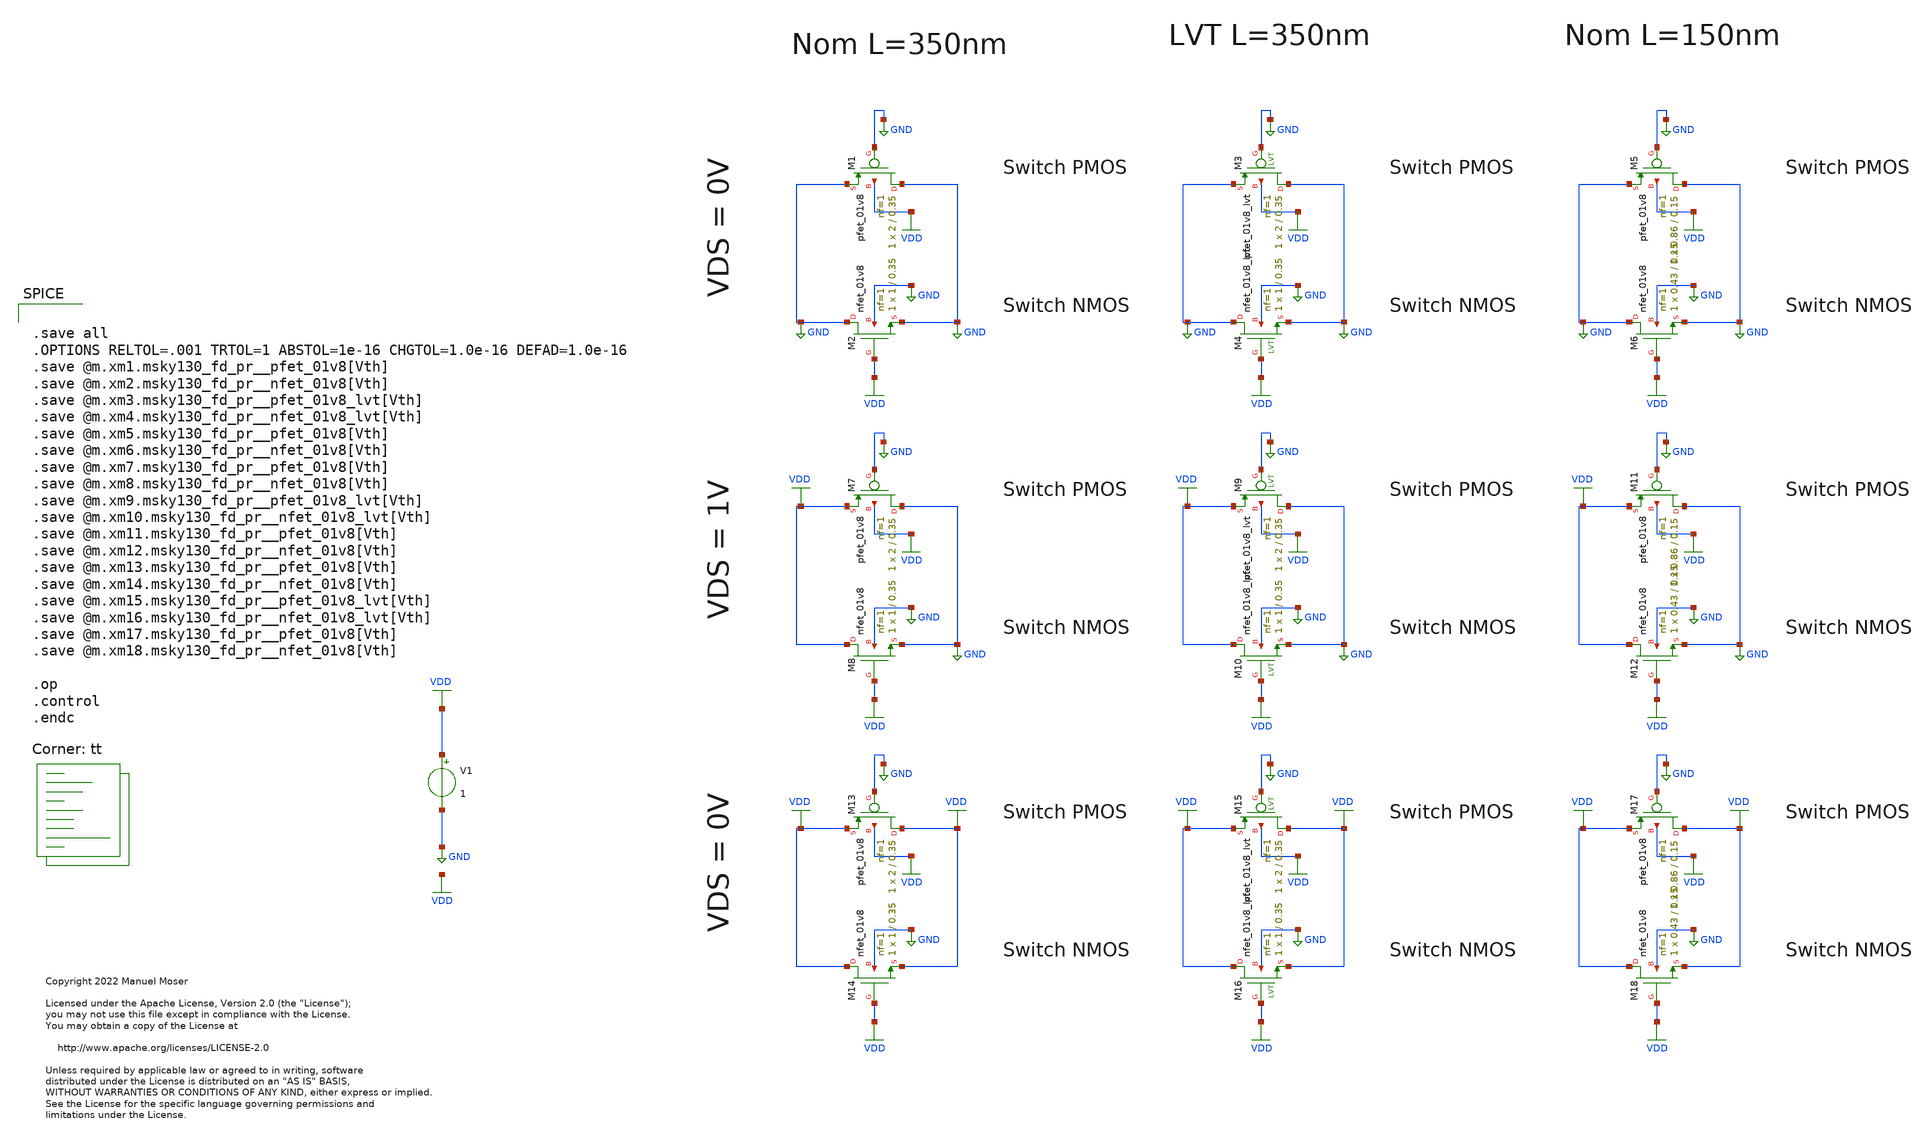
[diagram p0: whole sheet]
** sch_path: xschem/switch/switch_vth_tb.sch
* Copyright 2022 Manuel Moser
* Licensed under the Apache License, Version 2.0 (the "License");
**.subckt switch_vth_tb
V1 VDD GND 1
XM2 GND VDD GND GND sky130_fd_pr__nfet_01v8 L=0.35 W=1 nf=1 ad='int((nf+1)/2) * W/nf * 0.29' as='int((nf+2)/2) * W/nf * 0.29'
+ pd='2*int((nf+1)/2) * (W/nf + 0.29)' ps='2*int((nf+2)/2) * (W/nf + 0.29)' nrd='0.29 / W' nrs='0.29 / W'
+ sa=0 sb=0 sd=0 mult=1 m=1
XM1 GND GND GND VDD sky130_fd_pr__pfet_01v8 L=0.35 W=2 nf=1 ad='int((nf+1)/2) * W/nf * 0.29' as='int((nf+2)/2) * W/nf * 0.29'
+ pd='2*int((nf+1)/2) * (W/nf + 0.29)' ps='2*int((nf+2)/2) * (W/nf + 0.29)' nrd='0.29 / W' nrs='0.29 / W'
+ sa=0 sb=0 sd=0 mult=1 m=1
XM3 GND GND GND VDD sky130_fd_pr__pfet_01v8_lvt L=0.35 W=2 nf=1 ad='int((nf+1)/2) * W/nf * 0.29' as='int((nf+2)/2) * W/nf * 0.29'
+ pd='2*int((nf+1)/2) * (W/nf + 0.29)' ps='2*int((nf+2)/2) * (W/nf + 0.29)' nrd='0.29 / W' nrs='0.29 / W'
+ sa=0 sb=0 sd=0 mult=1 m=1
XM4 GND VDD GND GND sky130_fd_pr__nfet_01v8_lvt L=0.35 W=1 nf=1 ad='int((nf+1)/2) * W/nf * 0.29' as='int((nf+2)/2) * W/nf * 0.29'
+ pd='2*int((nf+1)/2) * (W/nf + 0.29)' ps='2*int((nf+2)/2) * (W/nf + 0.29)' nrd='0.29 / W' nrs='0.29 / W'
+ sa=0 sb=0 sd=0 mult=1 m=1
XM6 GND VDD GND GND sky130_fd_pr__nfet_01v8 L=0.15 W=0.43 nf=1 ad='int((nf+1)/2) * W/nf * 0.29' as='int((nf+2)/2) * W/nf * 0.29'
+ pd='2*int((nf+1)/2) * (W/nf + 0.29)' ps='2*int((nf+2)/2) * (W/nf + 0.29)' nrd='0.29 / W' nrs='0.29 / W'
+ sa=0 sb=0 sd=0 mult=1 m=1
XM5 GND GND GND VDD sky130_fd_pr__pfet_01v8 L=0.15 W=0.86 nf=1 ad='int((nf+1)/2) * W/nf * 0.29' as='int((nf+2)/2) * W/nf * 0.29'
+ pd='2*int((nf+1)/2) * (W/nf + 0.29)' ps='2*int((nf+2)/2) * (W/nf + 0.29)' nrd='0.29 / W' nrs='0.29 / W'
+ sa=0 sb=0 sd=0 mult=1 m=1
XM8 VDD VDD GND GND sky130_fd_pr__nfet_01v8 L=0.35 W=1 nf=1 ad='int((nf+1)/2) * W/nf * 0.29' as='int((nf+2)/2) * W/nf * 0.29'
+ pd='2*int((nf+1)/2) * (W/nf + 0.29)' ps='2*int((nf+2)/2) * (W/nf + 0.29)' nrd='0.29 / W' nrs='0.29 / W'
+ sa=0 sb=0 sd=0 mult=1 m=1
XM7 GND GND VDD VDD sky130_fd_pr__pfet_01v8 L=0.35 W=2 nf=1 ad='int((nf+1)/2) * W/nf * 0.29' as='int((nf+2)/2) * W/nf * 0.29'
+ pd='2*int((nf+1)/2) * (W/nf + 0.29)' ps='2*int((nf+2)/2) * (W/nf + 0.29)' nrd='0.29 / W' nrs='0.29 / W'
+ sa=0 sb=0 sd=0 mult=1 m=1
XM9 GND GND VDD VDD sky130_fd_pr__pfet_01v8_lvt L=0.35 W=2 nf=1 ad='int((nf+1)/2) * W/nf * 0.29' as='int((nf+2)/2) * W/nf * 0.29'
+ pd='2*int((nf+1)/2) * (W/nf + 0.29)' ps='2*int((nf+2)/2) * (W/nf + 0.29)' nrd='0.29 / W' nrs='0.29 / W'
+ sa=0 sb=0 sd=0 mult=1 m=1
XM10 VDD VDD GND GND sky130_fd_pr__nfet_01v8_lvt L=0.35 W=1 nf=1 ad='int((nf+1)/2) * W/nf * 0.29' as='int((nf+2)/2) * W/nf * 0.29'
+ pd='2*int((nf+1)/2) * (W/nf + 0.29)' ps='2*int((nf+2)/2) * (W/nf + 0.29)' nrd='0.29 / W' nrs='0.29 / W'
+ sa=0 sb=0 sd=0 mult=1 m=1
XM12 VDD VDD GND GND sky130_fd_pr__nfet_01v8 L=0.15 W=0.43 nf=1 ad='int((nf+1)/2) * W/nf * 0.29' as='int((nf+2)/2) * W/nf * 0.29'
+ pd='2*int((nf+1)/2) * (W/nf + 0.29)' ps='2*int((nf+2)/2) * (W/nf + 0.29)' nrd='0.29 / W' nrs='0.29 / W'
+ sa=0 sb=0 sd=0 mult=1 m=1
XM11 GND GND VDD VDD sky130_fd_pr__pfet_01v8 L=0.15 W=0.86 nf=1 ad='int((nf+1)/2) * W/nf * 0.29' as='int((nf+2)/2) * W/nf * 0.29'
+ pd='2*int((nf+1)/2) * (W/nf + 0.29)' ps='2*int((nf+2)/2) * (W/nf + 0.29)' nrd='0.29 / W' nrs='0.29 / W'
+ sa=0 sb=0 sd=0 mult=1 m=1
XM14 VDD VDD VDD GND sky130_fd_pr__nfet_01v8 L=0.35 W=1 nf=1 ad='int((nf+1)/2) * W/nf * 0.29' as='int((nf+2)/2) * W/nf * 0.29'
+ pd='2*int((nf+1)/2) * (W/nf + 0.29)' ps='2*int((nf+2)/2) * (W/nf + 0.29)' nrd='0.29 / W' nrs='0.29 / W'
+ sa=0 sb=0 sd=0 mult=1 m=1
XM13 VDD GND VDD VDD sky130_fd_pr__pfet_01v8 L=0.35 W=2 nf=1 ad='int((nf+1)/2) * W/nf * 0.29' as='int((nf+2)/2) * W/nf * 0.29'
+ pd='2*int((nf+1)/2) * (W/nf + 0.29)' ps='2*int((nf+2)/2) * (W/nf + 0.29)' nrd='0.29 / W' nrs='0.29 / W'
+ sa=0 sb=0 sd=0 mult=1 m=1
XM15 VDD GND VDD VDD sky130_fd_pr__pfet_01v8_lvt L=0.35 W=2 nf=1 ad='int((nf+1)/2) * W/nf * 0.29' as='int((nf+2)/2) * W/nf * 0.29'
+ pd='2*int((nf+1)/2) * (W/nf + 0.29)' ps='2*int((nf+2)/2) * (W/nf + 0.29)' nrd='0.29 / W' nrs='0.29 / W'
+ sa=0 sb=0 sd=0 mult=1 m=1
XM16 VDD VDD VDD GND sky130_fd_pr__nfet_01v8_lvt L=0.35 W=1 nf=1 ad='int((nf+1)/2) * W/nf * 0.29' as='int((nf+2)/2) * W/nf * 0.29'
+ pd='2*int((nf+1)/2) * (W/nf + 0.29)' ps='2*int((nf+2)/2) * (W/nf + 0.29)' nrd='0.29 / W' nrs='0.29 / W'
+ sa=0 sb=0 sd=0 mult=1 m=1
XM18 VDD VDD VDD GND sky130_fd_pr__nfet_01v8 L=0.15 W=0.43 nf=1 ad='int((nf+1)/2) * W/nf * 0.29' as='int((nf+2)/2) * W/nf * 0.29'
+ pd='2*int((nf+1)/2) * (W/nf + 0.29)' ps='2*int((nf+2)/2) * (W/nf + 0.29)' nrd='0.29 / W' nrs='0.29 / W'
+ sa=0 sb=0 sd=0 mult=1 m=1
XM17 VDD GND VDD VDD sky130_fd_pr__pfet_01v8 L=0.15 W=0.86 nf=1 ad='int((nf+1)/2) * W/nf * 0.29' as='int((nf+2)/2) * W/nf * 0.29'
+ pd='2*int((nf+1)/2) * (W/nf + 0.29)' ps='2*int((nf+2)/2) * (W/nf + 0.29)' nrd='0.29 / W' nrs='0.29 / W'
+ sa=0 sb=0 sd=0 mult=1 m=1
**** begin user architecture code


.save all
.OPTIONS RELTOL=.001 TRTOL=1 ABSTOL=1e-16 CHGTOL=1.0e-16 DEFAD=1.0e-16
.save @m.xm1.msky130_fd_pr__pfet_01v8[Vth]
.save @m.xm2.msky130_fd_pr__nfet_01v8[Vth]
.save @m.xm3.msky130_fd_pr__pfet_01v8_lvt[Vth]
.save @m.xm4.msky130_fd_pr__nfet_01v8_lvt[Vth]
.save @m.xm5.msky130_fd_pr__pfet_01v8[Vth]
.save @m.xm6.msky130_fd_pr__nfet_01v8[Vth]
.save @m.xm7.msky130_fd_pr__pfet_01v8[Vth]
.save @m.xm8.msky130_fd_pr__nfet_01v8[Vth]
.save @m.xm9.msky130_fd_pr__pfet_01v8_lvt[Vth]
.save @m.xm10.msky130_fd_pr__nfet_01v8_lvt[Vth]
.save @m.xm11.msky130_fd_pr__pfet_01v8[Vth]
.save @m.xm12.msky130_fd_pr__nfet_01v8[Vth]
.save @m.xm13.msky130_fd_pr__pfet_01v8[Vth]
.save @m.xm14.msky130_fd_pr__nfet_01v8[Vth]
.save @m.xm15.msky130_fd_pr__pfet_01v8_lvt[Vth]
.save @m.xm16.msky130_fd_pr__nfet_01v8_lvt[Vth]
.save @m.xm17.msky130_fd_pr__pfet_01v8[Vth]
.save @m.xm18.msky130_fd_pr__nfet_01v8[Vth]

.op
.control
.endc


.lib $::SKYWATER_MODELS/sky130.lib.spice tt
**** end user architecture code
**.ends
.GLOBAL GND
.GLOBAL VDD
.end
